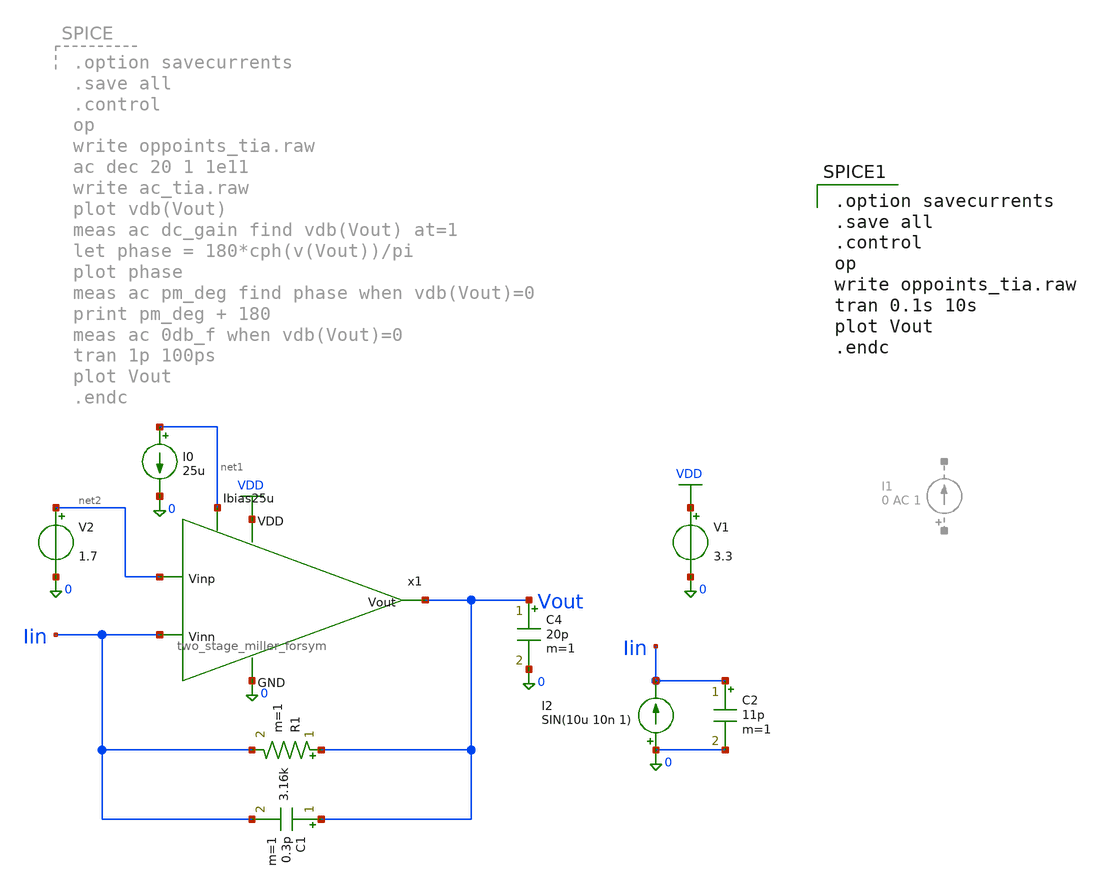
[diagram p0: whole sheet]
** sch_path: jz_tia/tia.sch
**.subckt tia
I0 net1 0 25u
V1 VDD 0 3.3
R1 Vout Iin 3.16k m=1
C1 Vout Iin 0.3p m=1
C2 Iin 0 11p m=1
C4 Vout 0 20p m=1
x1 VDD Vout net2 Iin net1 0 two_stage_miller_forsym
I2 0 Iin SIN(10u 10n 1)
V2 net2 0 1.7
**** begin user architecture code

.include $::180MCU_MODELS/design.ngspice
.lib $::180MCU_MODELS/sm141064.ngspice typical
.lib $::180MCU_MODELS/smbb000149.ngspice typical


.option savecurrents
.save all
.control
op
write oppoints_tia.raw
tran 0.1s 10s
plot Vout
.endc

**** end user architecture code
**.ends

* expanding   symbol:  chipathon-2026-ppg/jz_tia/two_stage_miller_forsym.sym # of pins=6
** sym_path: jz_tia/xschem/two_stage_miller_forsym.sym
** sch_path: jz_tia/xschem/two_stage_miller_forsym.sch
.subckt two_stage_miller_forsym VDD Vout Vinp Vinn Ibias25u GND
*.ipin Vinn
*.ipin Vinp
*.opin Vout
*.ipin Ibias25u
*.ipin VDD
*.ipin GND
XM1 net3 net3 GND GND nfet_03v3 L=1u W=1u nf=1 ad='int((nf+1)/2) * W/nf * 0.18u' as='int((nf+2)/2) * W/nf * 0.18u'
+ pd='2*int((nf+1)/2) * (W/nf + 0.18u)' ps='2*int((nf+2)/2) * (W/nf + 0.18u)' nrd='0.18u / W' nrs='0.18u / W'
+ sa=0 sb=0 sd=0 m=1
XM2 net2 net3 GND GND nfet_03v3 L=1u W=1u nf=1 ad='int((nf+1)/2) * W/nf * 0.18u' as='int((nf+2)/2) * W/nf * 0.18u'
+ pd='2*int((nf+1)/2) * (W/nf + 0.18u)' ps='2*int((nf+2)/2) * (W/nf + 0.18u)' nrd='0.18u / W' nrs='0.18u / W'
+ sa=0 sb=0 sd=0 m=1
XM3 net1 Ibias25u VDD VDD pfet_03v3 L=1u W=14.7u nf=1 ad='int((nf+1)/2) * W/nf * 0.18u' as='int((nf+2)/2) * W/nf * 0.18u'
+ pd='2*int((nf+1)/2) * (W/nf + 0.18u)' ps='2*int((nf+2)/2) * (W/nf + 0.18u)' nrd='0.18u / W' nrs='0.18u / W'
+ sa=0 sb=0 sd=0 m=1
XM4 net3 Vinn net1 VDD pfet_03v3 L=1u W=7.4u nf=1 ad='int((nf+1)/2) * W/nf * 0.18u' as='int((nf+2)/2) * W/nf * 0.18u'
+ pd='2*int((nf+1)/2) * (W/nf + 0.18u)' ps='2*int((nf+2)/2) * (W/nf + 0.18u)' nrd='0.18u / W' nrs='0.18u / W'
+ sa=0 sb=0 sd=0 m=1
XM5 net2 Vinp net1 VDD pfet_03v3 L=1u W=7.4u nf=1 ad='int((nf+1)/2) * W/nf * 0.18u' as='int((nf+2)/2) * W/nf * 0.18u'
+ pd='2*int((nf+1)/2) * (W/nf + 0.18u)' ps='2*int((nf+2)/2) * (W/nf + 0.18u)' nrd='0.18u / W' nrs='0.18u / W'
+ sa=0 sb=0 sd=0 m=1
XM6 Vout Ibias25u VDD VDD pfet_03v3 L=0.5u W=12.1u nf=1 ad='int((nf+1)/2) * W/nf * 0.18u' as='int((nf+2)/2) * W/nf * 0.18u'
+ pd='2*int((nf+1)/2) * (W/nf + 0.18u)' ps='2*int((nf+2)/2) * (W/nf + 0.18u)' nrd='0.18u / W' nrs='0.18u / W'
+ sa=0 sb=0 sd=0 m=1
XM7 Vout net2 GND GND nfet_03v3 L=0.28u W=0.97u nf=1 ad='int((nf+1)/2) * W/nf * 0.18u' as='int((nf+2)/2) * W/nf * 0.18u'
+ pd='2*int((nf+1)/2) * (W/nf + 0.18u)' ps='2*int((nf+2)/2) * (W/nf + 0.18u)' nrd='0.18u / W' nrs='0.18u / W'
+ sa=0 sb=0 sd=0 m=1
XM8 Ibias25u Ibias25u VDD VDD pfet_03v3 L=1u W=14.7u nf=1 ad='int((nf+1)/2) * W/nf * 0.18u' as='int((nf+2)/2) * W/nf * 0.18u'
+ pd='2*int((nf+1)/2) * (W/nf + 0.18u)' ps='2*int((nf+2)/2) * (W/nf + 0.18u)' nrd='0.18u / W' nrs='0.18u / W'
+ sa=0 sb=0 sd=0 m=1
C1 net2 net4 5p m=1
R1 net4 Vout 11k m=1
.ends

.GLOBAL VDD
.end
